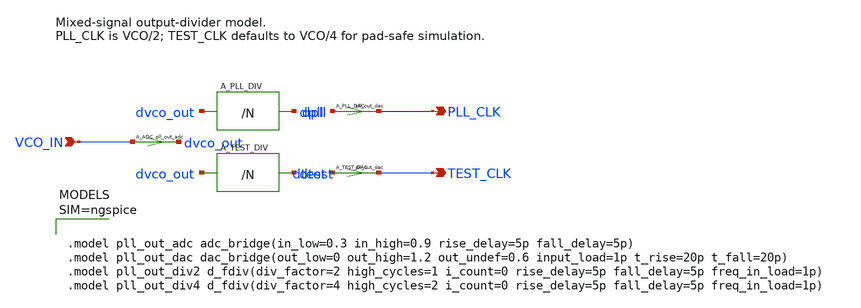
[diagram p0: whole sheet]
** sch_path: schematic/xschem/pll/output_divider.sch
**.subckt output_divider VCO_IN PLL_CLK TEST_CLK
*.ipin VCO_IN
*.opin PLL_CLK
*.opin TEST_CLK
A_ADC [ VCO_IN ] [ dvco_out ] pll_out_adc
A_PLL_DIV dvco_out dpll pll_out_div2
A_PLL_DAC [ dpll ] [ PLL_CLK ] pll_out_dac
A_TEST_DIV dvco_out dtest pll_out_div4
A_TEST_DAC [ dtest ] [ TEST_CLK ] pll_out_dac
**** begin user architecture code



.model pll_out_adc adc_bridge(in_low=0.3 in_high=0.9 rise_delay=5p fall_delay=5p)
.model pll_out_dac dac_bridge(out_low=0 out_high=1.2 out_undef=0.6 input_load=1p t_rise=20p
+ t_fall=20p)
.model pll_out_div2 d_fdiv(div_factor=2 high_cycles=1 i_count=0 rise_delay=5p fall_delay=5p
+ freq_in_load=1p)
.model pll_out_div4 d_fdiv(div_factor=4 high_cycles=2 i_count=0 rise_delay=5p fall_delay=5p
+ freq_in_load=1p)



**** end user architecture code
**.ends
.end
